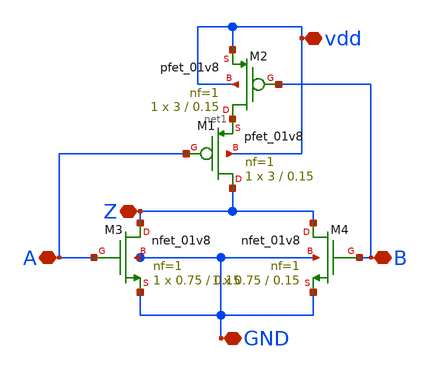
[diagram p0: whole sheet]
** sch_path: Todos los archivos para comparar/nor.sch
**.subckt nor GND A B vdd Z
*.iopin GND
*.iopin A
*.iopin B
*.iopin vdd
*.iopin Z
XM1 Z A net1 vdd sky130_fd_pr__pfet_01v8 L=0.15 W=3 nf=1 ad='int((nf+1)/2) * W/nf * 0.29' as='int((nf+2)/2) * W/nf * 0.29'
+ pd='2*int((nf+1)/2) * (W/nf + 0.29)' ps='2*int((nf+2)/2) * (W/nf + 0.29)' nrd='0.29 / W' nrs='0.29 / W'
+ sa=0 sb=0 sd=0 mult=1 m=1
XM2 net1 B vdd vdd sky130_fd_pr__pfet_01v8 L=0.15 W=3 nf=1 ad='int((nf+1)/2) * W/nf * 0.29' as='int((nf+2)/2) * W/nf * 0.29'
+ pd='2*int((nf+1)/2) * (W/nf + 0.29)' ps='2*int((nf+2)/2) * (W/nf + 0.29)' nrd='0.29 / W' nrs='0.29 / W'
+ sa=0 sb=0 sd=0 mult=1 m=1
XM3 Z A GND GND sky130_fd_pr__nfet_01v8 L=0.15 W=0.75 nf=1 ad='int((nf+1)/2) * W/nf * 0.29' as='int((nf+2)/2) * W/nf * 0.29'
+ pd='2*int((nf+1)/2) * (W/nf + 0.29)' ps='2*int((nf+2)/2) * (W/nf + 0.29)' nrd='0.29 / W' nrs='0.29 / W'
+ sa=0 sb=0 sd=0 mult=1 m=1
XM4 Z B GND GND sky130_fd_pr__nfet_01v8 L=0.15 W=0.75 nf=1 ad='int((nf+1)/2) * W/nf * 0.29' as='int((nf+2)/2) * W/nf * 0.29'
+ pd='2*int((nf+1)/2) * (W/nf + 0.29)' ps='2*int((nf+2)/2) * (W/nf + 0.29)' nrd='0.29 / W' nrs='0.29 / W'
+ sa=0 sb=0 sd=0 mult=1 m=1
**.ends
.end
